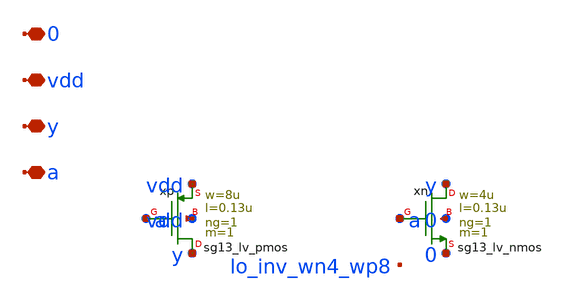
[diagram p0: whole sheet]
** sch_path: analog/lo/sch/lo_inv_4_8.sch
**.subckt lo_inv_4_8 a y vdd 0
*.iopin a
*.iopin y
*.iopin vdd
*.iopin 0
Xxp y a vdd vdd sg13_lv_pmos w=8u l=0.13u ng=1 m=1 mm_ok=1
Xxn y a 0 0 sg13_lv_nmos w=4u l=0.13u ng=1 m=1 mm_ok=1
**.ends
.end
